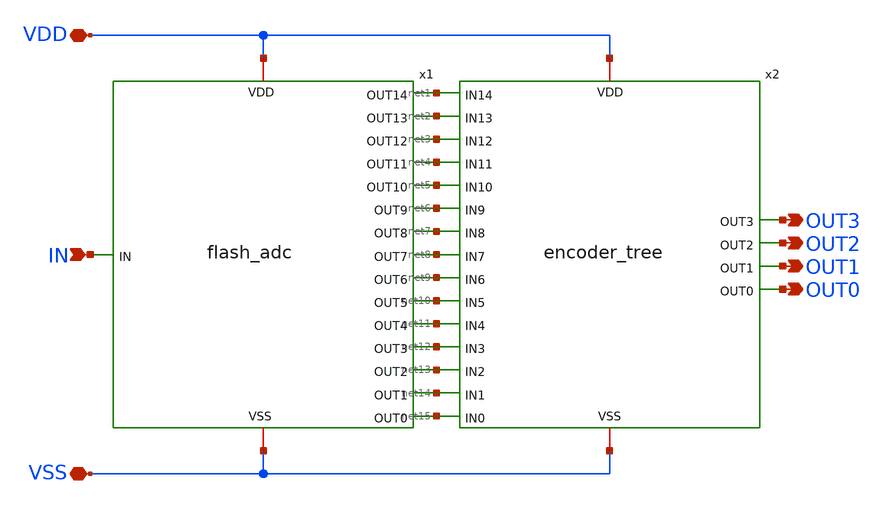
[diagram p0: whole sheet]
** sch_path: xschem/adc_with_encoder.sch
**.subckt adc_with_encoder VDD VSS IN OUT0 OUT1 OUT2 OUT3
*.iopin VDD
*.iopin VSS
*.ipin IN
*.opin OUT0
*.opin OUT1
*.opin OUT2
*.opin OUT3
x1 VDD IN net1 net2 net3 net4 net5 net6 net7 net8 net9 net10 net11 net12 net13 net14 net15 VSS
+ flash_adc
x2 net1 VDD net2 net3 net4 net5 net6 net7 net8 OUT3 net9 OUT2 net10 OUT1 net11 OUT0 net12 net13
+ net14 VSS net15 encoder_tree
**.ends

* expanding   symbol:  flash_adc.sym # of pins=18
** sym_path: xschem/flash_adc.sym
** sch_path: xschem/flash_adc.sch
.subckt flash_adc VDD IN OUT14 OUT13 OUT12 OUT11 OUT10 OUT9 OUT8 OUT7 OUT6 OUT5 OUT4 OUT3 OUT2 OUT1
+ OUT0 VSS
*.iopin VDD
*.iopin VSS
*.ipin IN
*.opin OUT0
*.opin OUT1
*.opin OUT2
*.opin OUT3
*.opin OUT4
*.opin OUT5
*.opin OUT6
*.opin OUT7
*.opin OUT8
*.opin OUT9
*.opin OUT10
*.opin OUT11
*.opin OUT12
*.opin OUT13
*.opin OUT14
x1 VDD net2 IN VSS vfollower
x2 VDD net1 IN VSS vfollower
x3 VDD net3 IN VSS vfollower
x4 VDD net4 IN VSS vfollower
x5 net10 VDD net2 OUT0 VSS VSS ladder_rung
x6 net9 VDD net2 OUT1 VSS net10 ladder_rung
x7 net8 VDD net2 OUT2 VSS net9 ladder_rung
x8 net5 VDD net2 OUT3 VSS net8 ladder_rung
x9 net5 VDD net1 OUT4 VSS net11 ladder_rung
x10 net11 VDD net1 OUT5 VSS net12 ladder_rung
x11 net12 VDD net1 OUT6 VSS net13 ladder_rung
x12 net13 VDD net1 OUT7 VSS net7 ladder_rung
x13 net16 VDD net3 OUT8 VSS net7 ladder_rung
x14 net15 VDD net3 OUT9 VSS net16 ladder_rung
x15 net14 VDD net3 OUT10 VSS net15 ladder_rung
x16 net6 VDD net3 OUT11 VSS net14 ladder_rung
x17 net6 VDD net4 OUT12 VSS net17 ladder_rung
x18 net17 VDD net4 OUT13 VSS net18 ladder_rung
x19 net18 VDD net4 OUT14 VSS VDD ladder_rung
.ends


* expanding   symbol:  encoder_tree.sym # of pins=21
** sym_path: xschem/encoder_tree.sym
** sch_path: xschem/encoder_tree.sch
.subckt encoder_tree IN14 VDD IN13 IN12 IN11 IN10 IN9 IN8 IN7 OUT3 IN6 OUT2 IN5 OUT1 IN4 OUT0 IN3
+ IN2 IN1 VSS IN0
*.ipin IN0
*.ipin IN1
*.ipin IN2
*.ipin IN3
*.ipin IN4
*.ipin IN5
*.ipin IN6
*.ipin IN7
*.ipin IN8
*.ipin IN9
*.ipin IN10
*.ipin IN11
*.ipin IN12
*.ipin IN13
*.ipin IN14
*.opin OUT0
*.opin OUT1
*.opin OUT2
*.opin OUT3
*.iopin VDD
*.iopin VSS
x1 IN2 IN1 IN0 VSS VSS VDD VDD net3 sky130_fd_sc_hd__maj3_4
x2 IN4 IN3 IN2 VSS VSS VDD VDD net1 sky130_fd_sc_hd__maj3_4
x3 IN6 IN5 IN4 VSS VSS VDD VDD net4 sky130_fd_sc_hd__maj3_4
x4 IN8 IN7 IN6 VSS VSS VDD VDD net8 sky130_fd_sc_hd__maj3_4
x5 IN10 IN9 IN8 VSS VSS VDD VDD net9 sky130_fd_sc_hd__maj3_4
x6 IN12 IN11 IN10 VSS VSS VDD VDD net11 sky130_fd_sc_hd__maj3_4
x7 IN14 IN13 IN12 VSS VSS VDD VDD net10 sky130_fd_sc_hd__maj3_4
x8 IN0 IN2 net3 VSS VSS VDD VDD net7 sky130_fd_sc_hd__mux2_4
x9 IN4 IN6 net4 VSS VSS VDD VDD net6 sky130_fd_sc_hd__mux2_4
x10 IN8 IN10 net9 VSS VSS VDD VDD net13 sky130_fd_sc_hd__mux2_4
x11 IN12 IN14 net10 VSS VSS VDD VDD net14 sky130_fd_sc_hd__mux2_4
x12 net4 net1 net3 VSS VSS VDD VDD net2 sky130_fd_sc_hd__maj3_4
x13 net9 net8 net4 VSS VSS VDD VDD net15 sky130_fd_sc_hd__maj3_4
x14 net10 net11 net9 VSS VSS VDD VDD net12 sky130_fd_sc_hd__maj3_4
x15 net3 net4 net2 VSS VSS VDD VDD net5 sky130_fd_sc_hd__mux2_4
x16 net7 net6 net2 VSS VSS VDD VDD net18 sky130_fd_sc_hd__mux2_4
x17 net9 net10 net12 VSS VSS VDD VDD net16 sky130_fd_sc_hd__mux2_4
x18 net13 net14 net12 VSS VSS VDD VDD net17 sky130_fd_sc_hd__mux2_4
x19 net12 net15 net2 VSS VSS VDD VDD OUT3 sky130_fd_sc_hd__maj3_4
x20 net2 net12 OUT3 VSS VSS VDD VDD OUT2 sky130_fd_sc_hd__mux2_4
x21 net5 net16 OUT3 VSS VSS VDD VDD OUT1 sky130_fd_sc_hd__mux2_4
x22 net18 net17 OUT3 VSS VSS VDD VDD OUT0 sky130_fd_sc_hd__mux2_4
.ends


* expanding   symbol:  vfollower.sym # of pins=4
** sym_path: xschem/vfollower.sym
** sch_path: xschem/vfollower.sch
.subckt vfollower VDD OUT IN VSS
*.iopin VDD
*.iopin VSS
*.ipin IN
*.opin OUT
x1 VDD OUT IN OUT VSS opamp
.ends


* expanding   symbol:  ladder_rung.sym # of pins=6
** sym_path: xschem/ladder_rung.sym
** sch_path: xschem/ladder_rung.sch
.subckt ladder_rung REF2 VDD IN OUT VSS REF1
*.opin OUT
*.iopin VDD
*.iopin VSS
*.ipin IN
*.iopin REF1
*.iopin REF2
XR1 REF1 net1 VSS sky130_fd_pr__res_xhigh_po_0p35 L=2.34 mult=1 m=1
x5 VDD OUT IN net1 VSS comparator
XR2 net1 REF2 VSS sky130_fd_pr__res_xhigh_po_0p35 L=2.34 mult=1 m=1
.ends


* expanding   symbol:  opamp.sym # of pins=5
** sym_path: xschem/opamp.sym
** sch_path: xschem/opamp.sch
.subckt opamp VDD OUT P N VSS
*.iopin VDD
*.iopin VSS
*.ipin P
*.ipin N
*.opin OUT
XR1 net2 VDD VSS sky130_fd_pr__res_xhigh_po_0p35 L=24.36 mult=1 m=1
XM1 net2 net2 VSS VSS sky130_fd_pr__nfet_g5v0d10v5 L=1 W=2 nf=1 ad='int((nf+1)/2) * W/nf * 0.29' as='int((nf+2)/2) * W/nf * 0.29'
+ pd='2*int((nf+1)/2) * (W/nf + 0.29)' ps='2*int((nf+2)/2) * (W/nf + 0.29)' nrd='0.29 / W' nrs='0.29 / W'
+ sa=0 sb=0 sd=0 mult=2 m=2
XM7 net1 net1 VDD VDD sky130_fd_pr__pfet_g5v0d10v5 L=1 W=4 nf=1 ad='int((nf+1)/2) * W/nf * 0.29' as='int((nf+2)/2) * W/nf * 0.29'
+ pd='2*int((nf+1)/2) * (W/nf + 0.29)' ps='2*int((nf+2)/2) * (W/nf + 0.29)' nrd='0.29 / W' nrs='0.29 / W'
+ sa=0 sb=0 sd=0 mult=2 m=2
XM8 OUT net1 VDD VDD sky130_fd_pr__pfet_g5v0d10v5 L=1 W=4 nf=1 ad='int((nf+1)/2) * W/nf * 0.29' as='int((nf+2)/2) * W/nf * 0.29'
+ pd='2*int((nf+1)/2) * (W/nf + 0.29)' ps='2*int((nf+2)/2) * (W/nf + 0.29)' nrd='0.29 / W' nrs='0.29 / W'
+ sa=0 sb=0 sd=0 mult=2 m=2
XM4 net6 net2 VSS VSS sky130_fd_pr__nfet_g5v0d10v5 L=1 W=2 nf=1 ad='int((nf+1)/2) * W/nf * 0.29' as='int((nf+2)/2) * W/nf * 0.29'
+ pd='2*int((nf+1)/2) * (W/nf + 0.29)' ps='2*int((nf+2)/2) * (W/nf + 0.29)' nrd='0.29 / W' nrs='0.29 / W'
+ sa=0 sb=0 sd=0 mult=2 m=2
XM5 net1 P net6 VSS sky130_fd_pr__nfet_g5v0d10v5 L=1 W=2 nf=1 ad='int((nf+1)/2) * W/nf * 0.29' as='int((nf+2)/2) * W/nf * 0.29'
+ pd='2*int((nf+1)/2) * (W/nf + 0.29)' ps='2*int((nf+2)/2) * (W/nf + 0.29)' nrd='0.29 / W' nrs='0.29 / W'
+ sa=0 sb=0 sd=0 mult=2 m=2
XM6 OUT N net6 VSS sky130_fd_pr__nfet_g5v0d10v5 L=1 W=2 nf=1 ad='int((nf+1)/2) * W/nf * 0.29' as='int((nf+2)/2) * W/nf * 0.29'
+ pd='2*int((nf+1)/2) * (W/nf + 0.29)' ps='2*int((nf+2)/2) * (W/nf + 0.29)' nrd='0.29 / W' nrs='0.29 / W'
+ sa=0 sb=0 sd=0 mult=2 m=2
XM2 net5 net2 VSS VSS sky130_fd_pr__nfet_g5v0d10v5 L=1 W=2 nf=1 ad='int((nf+1)/2) * W/nf * 0.29' as='int((nf+2)/2) * W/nf * 0.29'
+ pd='2*int((nf+1)/2) * (W/nf + 0.29)' ps='2*int((nf+2)/2) * (W/nf + 0.29)' nrd='0.29 / W' nrs='0.29 / W'
+ sa=0 sb=0 sd=0 mult=2 m=2
XM9 net4 net5 VDD VDD sky130_fd_pr__pfet_g5v0d10v5 L=1 W=4 nf=1 ad='int((nf+1)/2) * W/nf * 0.29' as='int((nf+2)/2) * W/nf * 0.29'
+ pd='2*int((nf+1)/2) * (W/nf + 0.29)' ps='2*int((nf+2)/2) * (W/nf + 0.29)' nrd='0.29 / W' nrs='0.29 / W'
+ sa=0 sb=0 sd=0 mult=2 m=2
XM3 VDD net5 net5 VDD sky130_fd_pr__pfet_g5v0d10v5 L=1 W=4 nf=1 ad='int((nf+1)/2) * W/nf * 0.29' as='int((nf+2)/2) * W/nf * 0.29'
+ pd='2*int((nf+1)/2) * (W/nf + 0.29)' ps='2*int((nf+2)/2) * (W/nf + 0.29)' nrd='0.29 / W' nrs='0.29 / W'
+ sa=0 sb=0 sd=0 mult=2 m=2
XM10 net3 P net4 VDD sky130_fd_pr__pfet_g5v0d10v5 L=1 W=4 nf=1 ad='int((nf+1)/2) * W/nf * 0.29' as='int((nf+2)/2) * W/nf * 0.29'
+ pd='2*int((nf+1)/2) * (W/nf + 0.29)' ps='2*int((nf+2)/2) * (W/nf + 0.29)' nrd='0.29 / W' nrs='0.29 / W'
+ sa=0 sb=0 sd=0 mult=2 m=2
XM11 OUT N net4 VDD sky130_fd_pr__pfet_g5v0d10v5 L=1 W=4 nf=1 ad='int((nf+1)/2) * W/nf * 0.29' as='int((nf+2)/2) * W/nf * 0.29'
+ pd='2*int((nf+1)/2) * (W/nf + 0.29)' ps='2*int((nf+2)/2) * (W/nf + 0.29)' nrd='0.29 / W' nrs='0.29 / W'
+ sa=0 sb=0 sd=0 mult=2 m=2
XM12 net3 net3 VSS VSS sky130_fd_pr__nfet_g5v0d10v5 L=1 W=2 nf=1 ad='int((nf+1)/2) * W/nf * 0.29' as='int((nf+2)/2) * W/nf * 0.29'
+ pd='2*int((nf+1)/2) * (W/nf + 0.29)' ps='2*int((nf+2)/2) * (W/nf + 0.29)' nrd='0.29 / W' nrs='0.29 / W'
+ sa=0 sb=0 sd=0 mult=2 m=2
XM13 OUT net3 VSS VSS sky130_fd_pr__nfet_g5v0d10v5 L=1 W=2 nf=1 ad='int((nf+1)/2) * W/nf * 0.29' as='int((nf+2)/2) * W/nf * 0.29'
+ pd='2*int((nf+1)/2) * (W/nf + 0.29)' ps='2*int((nf+2)/2) * (W/nf + 0.29)' nrd='0.29 / W' nrs='0.29 / W'
+ sa=0 sb=0 sd=0 mult=2 m=2
.ends


* expanding   symbol:  comparator.sym # of pins=5
** sym_path: xschem/comparator.sym
** sch_path: xschem/comparator.sch
.subckt comparator VDD OUT P N VSS
*.iopin VDD
*.iopin VSS
*.ipin P
*.ipin N
*.opin OUT
x1 VDD net1 P N VSS opamp
x2 VDD OUT net1 VSS buffer
.ends


* expanding   symbol:  buffer.sym # of pins=4
** sym_path: xschem/buffer.sym
** sch_path: xschem/buffer.sch
.subckt buffer VDD OUT IN VSS
*.iopin VDD
*.iopin VSS
*.ipin IN
*.opin OUT
XM1 net1 IN VSS VSS sky130_fd_pr__nfet_g5v0d10v5 L=0.5 W=0.5 nf=1 ad='int((nf+1)/2) * W/nf * 0.29' as='int((nf+2)/2) * W/nf * 0.29'
+ pd='2*int((nf+1)/2) * (W/nf + 0.29)' ps='2*int((nf+2)/2) * (W/nf + 0.29)' nrd='0.29 / W' nrs='0.29 / W'
+ sa=0 sb=0 sd=0 mult=1 m=1
XM2 net1 IN VDD VDD sky130_fd_pr__pfet_g5v0d10v5 L=0.5 W=1 nf=1 ad='int((nf+1)/2) * W/nf * 0.29' as='int((nf+2)/2) * W/nf * 0.29'
+ pd='2*int((nf+1)/2) * (W/nf + 0.29)' ps='2*int((nf+2)/2) * (W/nf + 0.29)' nrd='0.29 / W' nrs='0.29 / W'
+ sa=0 sb=0 sd=0 mult=1 m=1
XM3 OUT net1 VSS VSS sky130_fd_pr__nfet_g5v0d10v5 L=0.5 W=0.5 nf=1 ad='int((nf+1)/2) * W/nf * 0.29' as='int((nf+2)/2) * W/nf * 0.29'
+ pd='2*int((nf+1)/2) * (W/nf + 0.29)' ps='2*int((nf+2)/2) * (W/nf + 0.29)' nrd='0.29 / W' nrs='0.29 / W'
+ sa=0 sb=0 sd=0 mult=1 m=1
XM4 OUT net1 VDD VDD sky130_fd_pr__pfet_g5v0d10v5 L=0.5 W=1 nf=1 ad='int((nf+1)/2) * W/nf * 0.29' as='int((nf+2)/2) * W/nf * 0.29'
+ pd='2*int((nf+1)/2) * (W/nf + 0.29)' ps='2*int((nf+2)/2) * (W/nf + 0.29)' nrd='0.29 / W' nrs='0.29 / W'
+ sa=0 sb=0 sd=0 mult=1 m=1
.ends

.end
